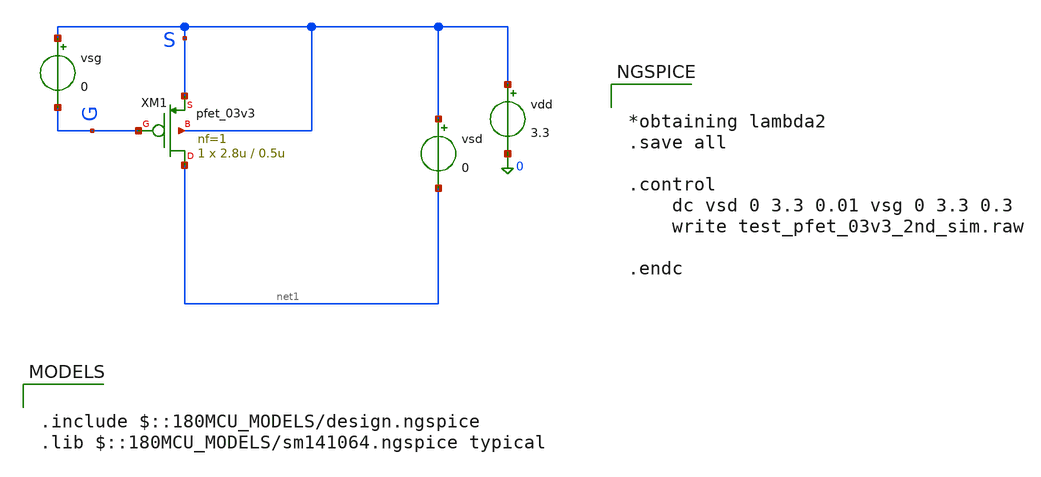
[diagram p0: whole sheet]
** sch_path: sch/integrator/test_pfet_03v3_2nd_sim.sch
**.subckt test_pfet_03v3_2nd_sim
XM1 net1 G S S pfet_03v3 L=0.5u W=2.8u nf=1 ad='int((nf+1)/2) * W/nf * 0.18u' as='int((nf+2)/2) * W/nf * 0.18u'
+ pd='2*int((nf+1)/2) * (W/nf + 0.18u)' ps='2*int((nf+2)/2) * (W/nf + 0.18u)' nrd='0.18u / W' nrs='0.18u / W'
+ sa=0 sb=0 sd=0 m=1
vsg S G 0
vdd S 0 3.3
vsd S net1 0
**** begin user architecture code


*obtaining lambda2
.save all

.control
	dc vsd 0 3.3 0.01 vsg 0 3.3 0.3
	write test_pfet_03v3_2nd_sim.raw

.endc



.include $::180MCU_MODELS/design.ngspice
.lib $::180MCU_MODELS/sm141064.ngspice typical

**** end user architecture code
**.ends
.end
